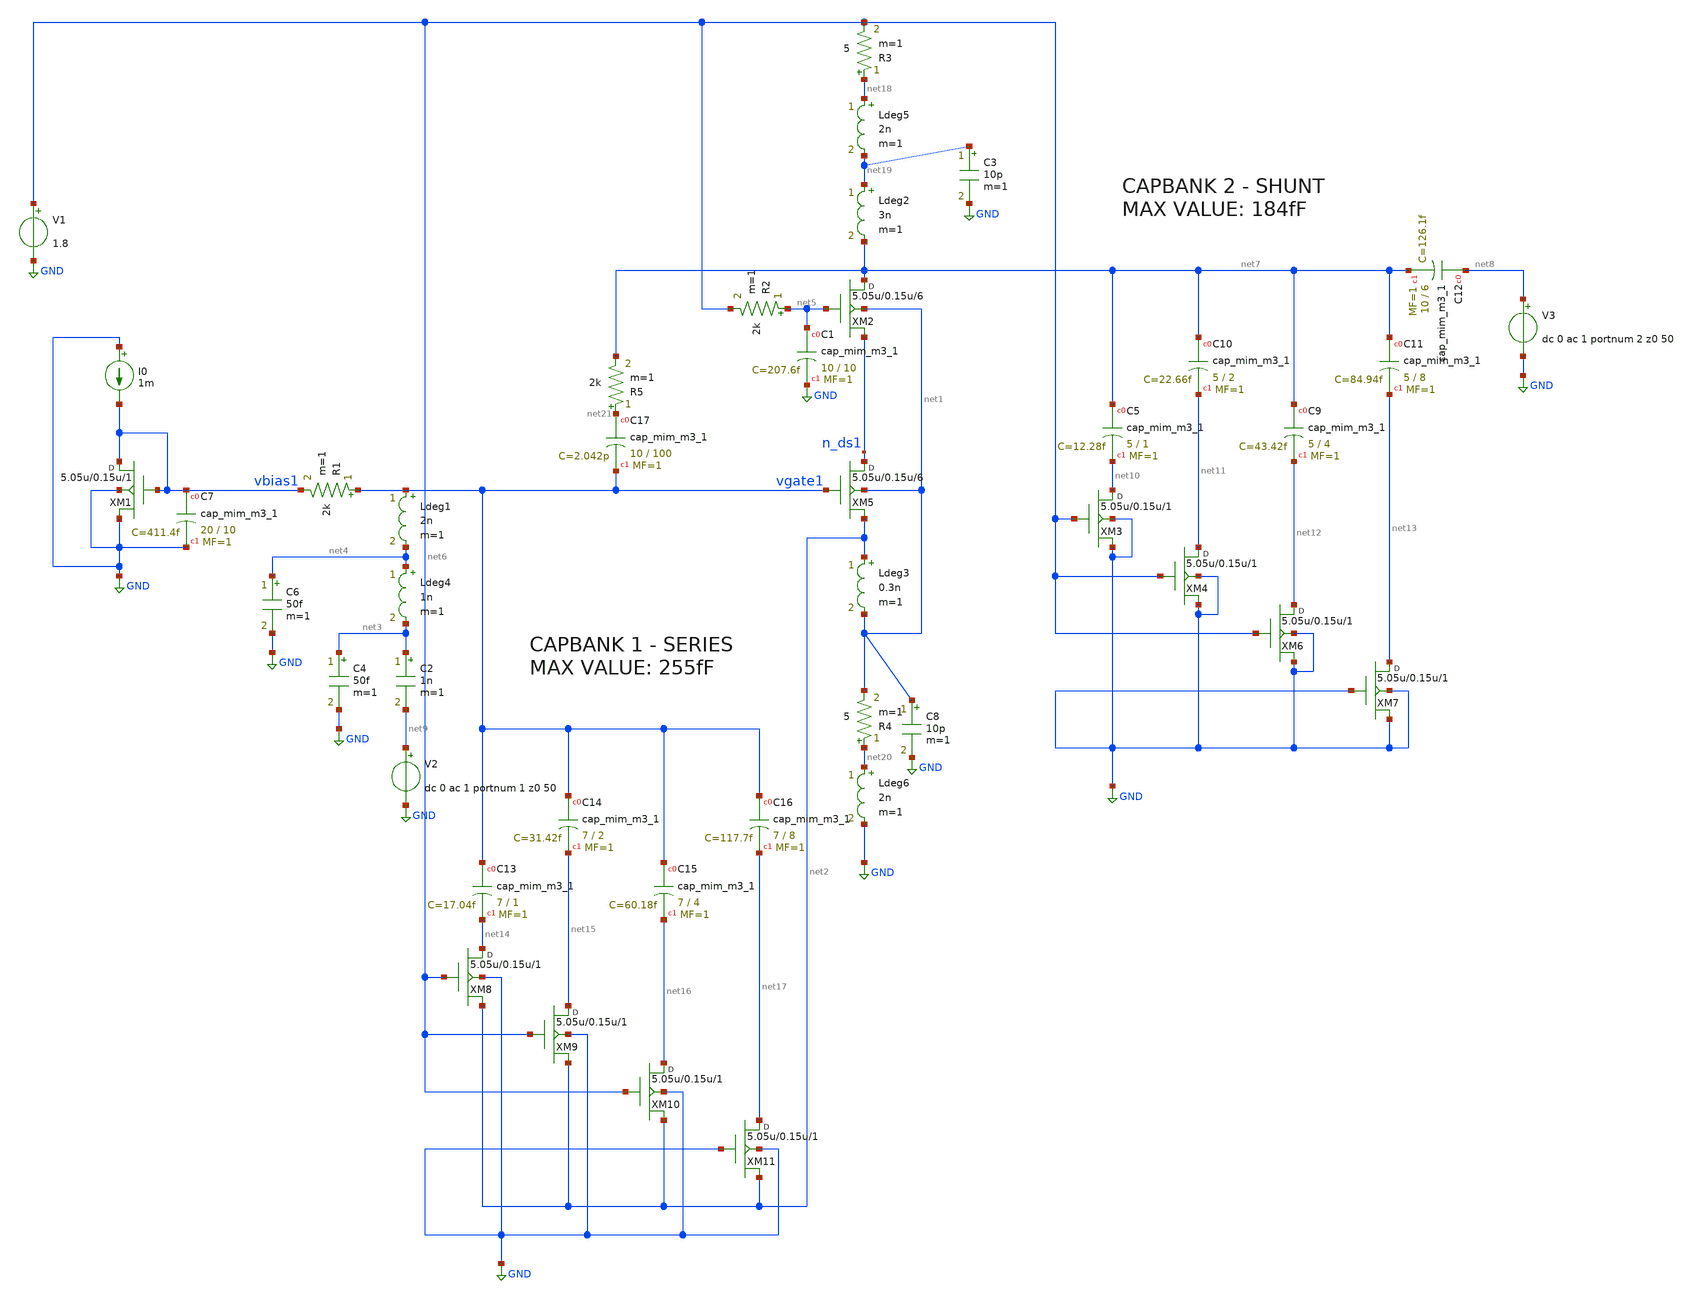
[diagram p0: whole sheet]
** sch_path: xschem/zptest.sch
**.subckt zptest
V1 net6 GND 1.8
V2 net9 GND dc 0 ac 1 portnum 1 z0 50
V3 net8 GND dc 0 ac 1 portnum 2 z0 50
Ldeg3 net2 net1 0.3n m=1
C2 net3 net9 1n m=1
R1 vgate1 vbias1 2k m=1
C4 net3 GND 50f m=1
Ldeg1 vgate1 net4 2n m=1
Ldeg4 net4 net3 1n m=1
C6 net4 GND 50f m=1
R2 net5 net6 2k m=1
I0 GND vbias1 1m
Ldeg2 net19 net7 3n m=1
XM5 n_ds1 vgate1 net2 net1 sky130_fd_pr__rf_nfet_01v8_bM04W5p00L0p15_ext w=5.05u l=0.15u m=6
XM1 vbias1 vbias1 GND GND sky130_fd_pr__rf_nfet_01v8_bM04W5p00L0p15_ext w=5.05u l=0.15u m=1
XM2 net7 net5 n_ds1 net1 sky130_fd_pr__rf_nfet_01v8_bM04W5p00L0p15_ext w=5.05u l=0.15u m=6
XC5 net7 net10 sky130_fd_pr__cap_mim_m3_1 W=5 L=1 MF=1 m=1
XC10 net7 net11 sky130_fd_pr__cap_mim_m3_1 W=5 L=2 MF=1 m=1
XC9 net7 net12 sky130_fd_pr__cap_mim_m3_1 W=5 L=4 MF=1 m=1
XC11 net7 net13 sky130_fd_pr__cap_mim_m3_1 W=5 L=8 MF=1 m=1
XM3 net10 net6 GND GND sky130_fd_pr__rf_nfet_01v8_bM04W5p00L0p15_ext w=5.05u l=0.15u m=1
XM4 net11 net6 GND GND sky130_fd_pr__rf_nfet_01v8_bM04W5p00L0p15_ext w=5.05u l=0.15u m=1
XM6 net12 net6 GND GND sky130_fd_pr__rf_nfet_01v8_bM04W5p00L0p15_ext w=5.05u l=0.15u m=1
XM7 net13 GND GND GND sky130_fd_pr__rf_nfet_01v8_bM04W5p00L0p15_ext w=5.05u l=0.15u m=1
XC12 net8 net7 sky130_fd_pr__cap_mim_m3_1 W=10 L=6 MF=1 m=1
XC1 net5 GND sky130_fd_pr__cap_mim_m3_1 W=10 L=10 MF=1 m=1
XC7 vbias1 GND sky130_fd_pr__cap_mim_m3_1 W=20 L=10 MF=1 m=1
XC13 vgate1 net14 sky130_fd_pr__cap_mim_m3_1 W=7 L=1 MF=1 m=1
XC14 vgate1 net15 sky130_fd_pr__cap_mim_m3_1 W=7 L=2 MF=1 m=1
XC15 vgate1 net16 sky130_fd_pr__cap_mim_m3_1 W=7 L=4 MF=1 m=1
XC16 vgate1 net17 sky130_fd_pr__cap_mim_m3_1 W=7 L=8 MF=1 m=1
XM8 net14 net6 net2 GND sky130_fd_pr__rf_nfet_01v8_bM04W5p00L0p15_ext w=5.05u l=0.15u m=1
XM9 net15 net6 net2 GND sky130_fd_pr__rf_nfet_01v8_bM04W5p00L0p15_ext w=5.05u l=0.15u m=1
XM10 net16 net6 net2 GND sky130_fd_pr__rf_nfet_01v8_bM04W5p00L0p15_ext w=5.05u l=0.15u m=1
XM11 net17 GND net2 GND sky130_fd_pr__rf_nfet_01v8_bM04W5p00L0p15_ext w=5.05u l=0.15u m=1
Ldeg5 net18 net19 2n m=1
R3 net18 net6 5 m=1
C3 net19 GND 10p m=1
Ldeg6 net20 GND 2n m=1
R4 net20 net1 5 m=1
C8 net1 GND 10p m=1
R5 net21 net7 2k m=1
XC17 net21 vgate1 sky130_fd_pr__cap_mim_m3_1 W=10 L=100 MF=1 m=1
**** begin user architecture code
.lib $::SKYWATER_MODELS/sky130.lib.spice tt
* .include $::PDKPATH/libs.ref/sky130_fd_sc_hvl/spice/sky130_fd_sc_hvl.spice



.subckt sky130_fd_pr__rf_nfet_01v8_bM04W5p00L0p15_ext DRAIN GATE SOURCE SUBSTRATE
X0 DRAIN GATE SOURCE SUBSTRATE sky130_fd_pr__nfet_01v8 ad=2.828e+12p pd=2.132e+07u as=4.242e+12p
+ ps=3.198e+07u w=5.05e+06u l=150000u
X1 SOURCE SUBSTRATE SUBSTRATE SUBSTRATE sky130_fd_pr__nfet_01v8 ad=0p pd=0u as=3.03e+12p
+ ps=2.14e+07u w=5.05e+06u l=150000u
X2 SOURCE GATE DRAIN SUBSTRATE sky130_fd_pr__nfet_01v8 ad=0p pd=0u as=0p ps=0u w=5.05e+06u l=150000u
X3 DRAIN GATE SOURCE SUBSTRATE sky130_fd_pr__nfet_01v8 ad=0p pd=0u as=0p ps=0u w=5.05e+06u l=150000u
X4 SUBSTRATE SUBSTRATE SOURCE SUBSTRATE sky130_fd_pr__nfet_01v8 ad=0p pd=0u as=0p ps=0u w=5.05e+06u
+ l=150000u
X5 SOURCE GATE DRAIN SUBSTRATE sky130_fd_pr__nfet_01v8 ad=0p pd=0u as=0p ps=0u w=5.05e+06u l=150000u
.ends
.sp dec 1000 1e9 10e9 1
* .ac dec 1000 0.01e9 100e9
.control
run
display

let S11 = S_1_1
let S21 = S_2_1
let S12 = S_1_2
let S22 = S_2_2

* Stability
let delta=S11*S22-S12*S21
let K    = (1-mag(S11)^2-mag(S22)^2+mag(delta)^2)/(2*mag(S12*S21))
let mu   = (1-mag(S11)^2)/(mag(S22-conj(S11)*delta)+mag(S21*S12))

let z11=50*(1+s_1_1)/(1-s_1_1)
let z22=50*(1+s_2_2)/(1-s_2_2)
plot real(z11) real(z22)
plot imag(z11) imag(z22)
plot db(S_1_1) db(S_2_2) db(S_2_1)

plot mag(delta)
plot (K)
plot (mu)
.endc


**** end user architecture code
**.ends
.GLOBAL GND
.end
